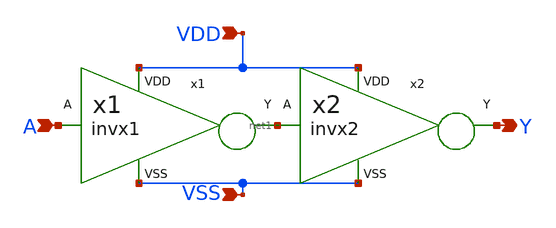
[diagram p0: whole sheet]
** sch_path: buffer/design_circuit/buf.sch
**.subckt buf A Y VDD VSS
*.ipin A
*.opin Y
*.ipin VDD
*.ipin VSS
x1 A net1 VDD VSS invx1
x2 net1 Y VDD VSS invx2
**.ends

* expanding   symbol:  invx1.sym # of pins=4
** sym_path: buffer/design_circuit/invx1.sym
** sch_path: buffer/design_circuit/invx1.sch
.subckt invx1 A Y VDD VSS
*.ipin A
*.opin Y
*.ipin VDD
*.ipin VSS
XM1 Y A VDD VDD sky130_fd_pr__pfet_01v8 L=0.15 W=1 nf=1 ad='int((nf+1)/2) * W/nf * 0.29' as='int((nf+2)/2) * W/nf * 0.29'
+ pd='2*int((nf+1)/2) * (W/nf + 0.29)' ps='2*int((nf+2)/2) * (W/nf + 0.29)' nrd='0.29 / W' nrs='0.29 / W'
+ sa=0 sb=0 sd=0 mult=1 m=1
XM2 Y A VSS VSS sky130_fd_pr__nfet_01v8 L=0.15 W=0.42 nf=1 ad='int((nf+1)/2) * W/nf * 0.29' as='int((nf+2)/2) * W/nf * 0.29'
+ pd='2*int((nf+1)/2) * (W/nf + 0.29)' ps='2*int((nf+2)/2) * (W/nf + 0.29)' nrd='0.29 / W' nrs='0.29 / W'
+ sa=0 sb=0 sd=0 mult=1 m=1
.ends


* expanding   symbol:  invx2.sym # of pins=4
** sym_path: buffer/design_circuit/invx2.sym
** sch_path: buffer/design_circuit/invx2.sch
.subckt invx2 A Y VDD VSS
*.ipin A
*.opin Y
*.ipin VDD
*.ipin VSS
XM1 Y A VDD VDD sky130_fd_pr__pfet_01v8 L=0.15 W=2 nf=1 ad='int((nf+1)/2) * W/nf * 0.29' as='int((nf+2)/2) * W/nf * 0.29'
+ pd='2*int((nf+1)/2) * (W/nf + 0.29)' ps='2*int((nf+2)/2) * (W/nf + 0.29)' nrd='0.29 / W' nrs='0.29 / W'
+ sa=0 sb=0 sd=0 mult=1 m=1
XM2 Y A VSS VSS sky130_fd_pr__nfet_01v8 L=0.15 W=0.84 nf=1 ad='int((nf+1)/2) * W/nf * 0.29' as='int((nf+2)/2) * W/nf * 0.29'
+ pd='2*int((nf+1)/2) * (W/nf + 0.29)' ps='2*int((nf+2)/2) * (W/nf + 0.29)' nrd='0.29 / W' nrs='0.29 / W'
+ sa=0 sb=0 sd=0 mult=1 m=1
.ends

.end
